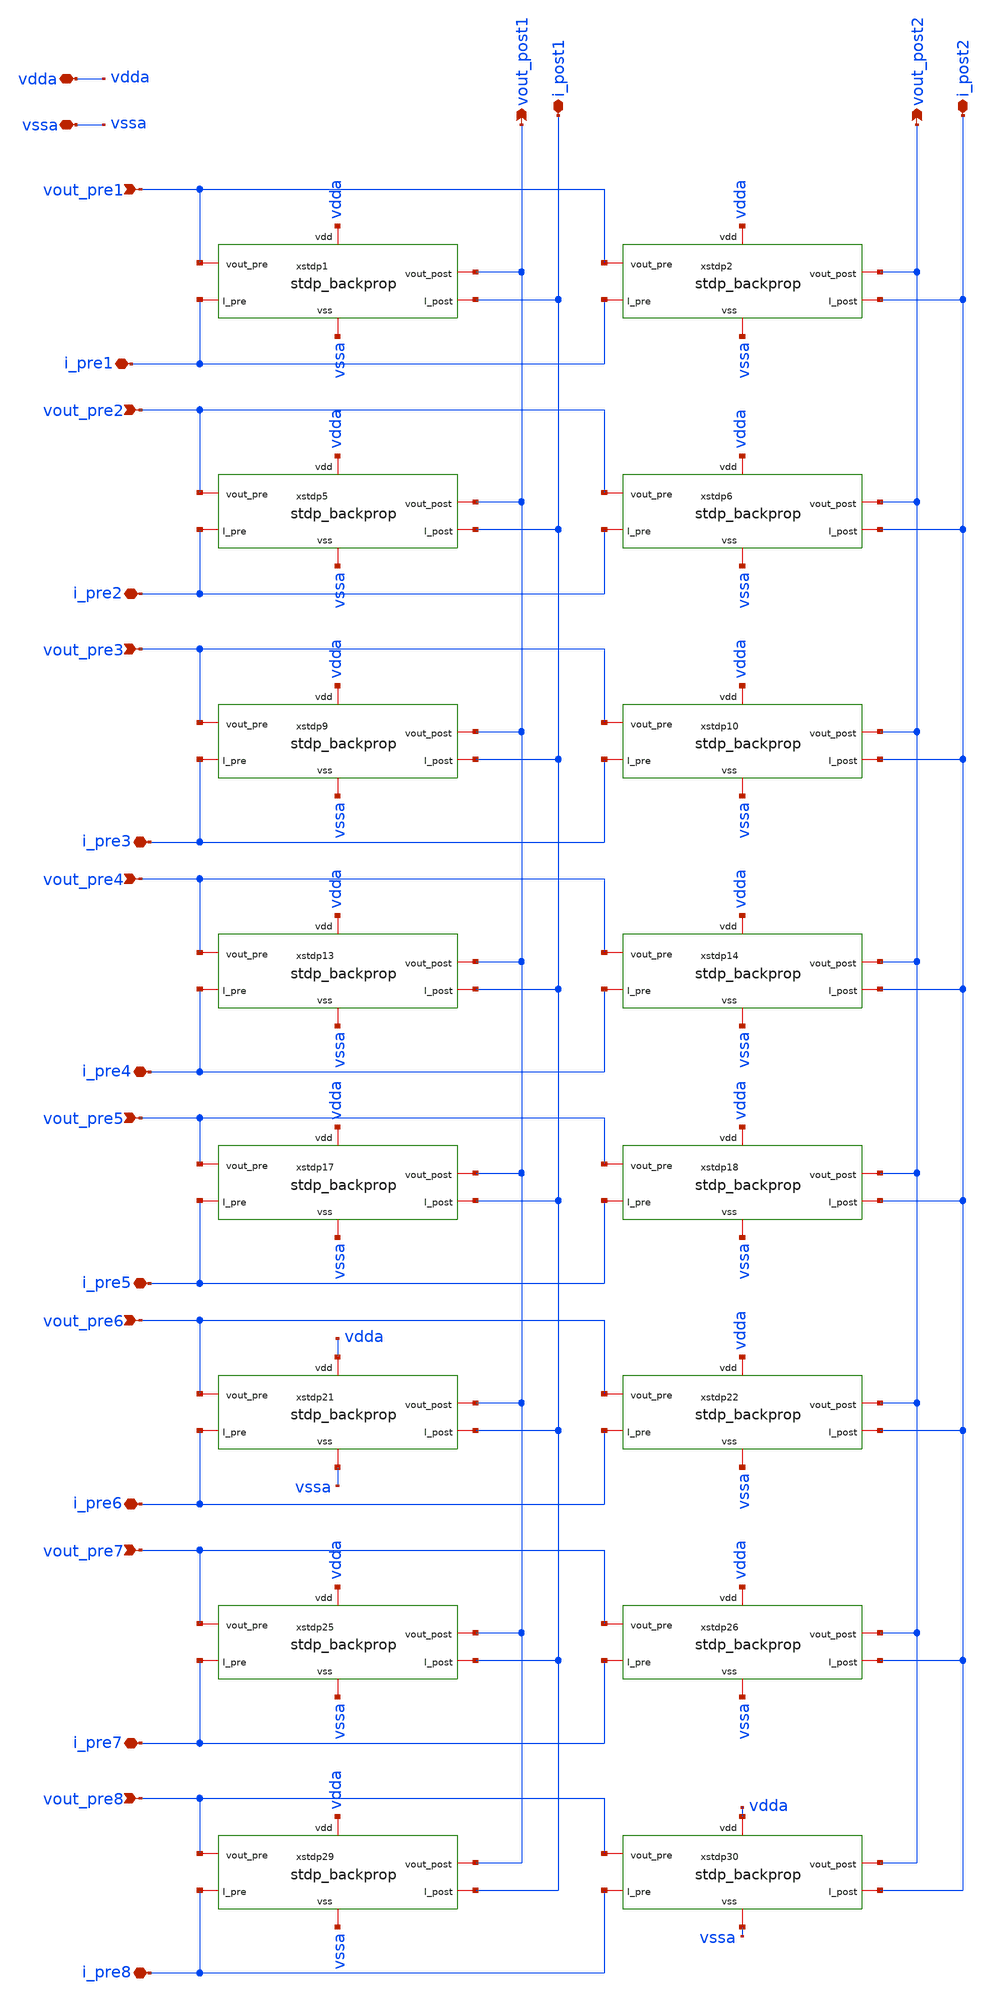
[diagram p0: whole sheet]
** sch_path: Synapse/stdp_backprop_8x2.sch
**.subckt stdp_backprop_8x2 vout_pre1 vout_post1 vdda vssa i_post1 vout_pre2 vout_pre3 vout_pre4
*+ vout_post2 i_post2 vout_pre5 vout_pre6 vout_pre7 vout_pre8 i_pre1 i_pre2 i_pre3 i_pre4 i_pre5 i_pre6 i_pre7
*+ i_pre8
*.ipin vout_pre1
*.opin vout_post1
*.iopin vdda
*.iopin vssa
*.iopin i_post1
*.ipin vout_pre2
*.ipin vout_pre3
*.ipin vout_pre4
*.opin vout_post2
*.iopin i_post2
*.ipin vout_pre5
*.ipin vout_pre6
*.ipin vout_pre7
*.ipin vout_pre8
*.iopin i_pre1
*.iopin i_pre2
*.iopin i_pre3
*.iopin i_pre4
*.iopin i_pre5
*.iopin i_pre6
*.iopin i_pre7
*.iopin i_pre8
xstdp2 vdda vssa vout_pre1 vout_post2 i_post2 i_pre1 stdp_backprop
xstdp5 vdda vssa vout_pre2 vout_post1 i_post1 i_pre2 stdp_backprop
xstdp6 vdda vssa vout_pre2 vout_post2 i_post2 i_pre2 stdp_backprop
xstdp9 vdda vssa vout_pre3 vout_post1 i_post1 i_pre3 stdp_backprop
xstdp10 vdda vssa vout_pre3 vout_post2 i_post2 i_pre3 stdp_backprop
xstdp13 vdda vssa vout_pre4 vout_post1 i_post1 i_pre4 stdp_backprop
xstdp14 vdda vssa vout_pre4 vout_post2 i_post2 i_pre4 stdp_backprop
xstdp17 vdda vssa vout_pre5 vout_post1 i_post1 i_pre5 stdp_backprop
xstdp18 vdda vssa vout_pre5 vout_post2 i_post2 i_pre5 stdp_backprop
xstdp21 vdda vssa vout_pre6 vout_post1 i_post1 i_pre6 stdp_backprop
xstdp22 vdda vssa vout_pre6 vout_post2 i_post2 i_pre6 stdp_backprop
xstdp25 vdda vssa vout_pre7 vout_post1 i_post1 i_pre7 stdp_backprop
xstdp26 vdda vssa vout_pre7 vout_post2 i_post2 i_pre7 stdp_backprop
xstdp29 vdda vssa vout_pre8 vout_post1 i_post1 i_pre8 stdp_backprop
xstdp30 vdda vssa vout_pre8 vout_post2 i_post2 i_pre8 stdp_backprop
xstdp1 vdda vssa vout_pre1 vout_post1 i_post1 i_pre1 stdp_backprop
**.ends
.end
